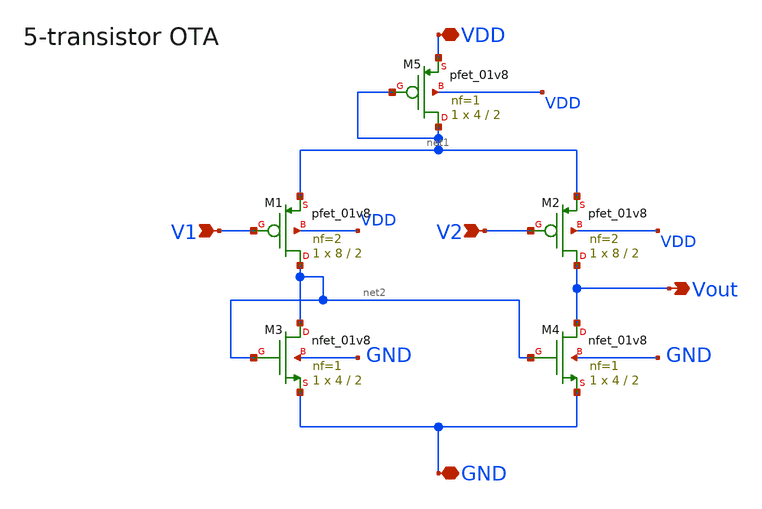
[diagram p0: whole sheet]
** sch_path: src/ota.sch
**.subckt ota VDD GND V2 V1 Vout
*.iopin VDD
*.iopin GND
*.ipin V2
*.ipin V1
*.opin Vout
XM1 net2 V1 net1 VDD sky130_fd_pr__pfet_01v8 L=2 W=8 nf=2 ad='int((2 + 1)/2) * 8 / 2 * 0.29' as='int((2 + 2)/2) * 8 / 2 * 0.29'
+ pd='2*int((2 + 1)/2) * (8 / 2 + 0.29)' ps='2*int((2 + 2)/2) * (8 / 2 + 0.29)' nrd='0.29 / 8 ' nrs='0.29 / 8 '
+ sa=0 sb=0 sd=0 mult=1 m=1
XM3 net2 net2 GND GND sky130_fd_pr__nfet_01v8 L=2 W=4 nf=1 ad='int((1 + 1)/2) * 4 / 1 * 0.29' as='int((1 + 2)/2) * 4 / 1 * 0.29'
+ pd='2*int((1 + 1)/2) * (4 / 1 + 0.29)' ps='2*int((1 + 2)/2) * (4 / 1 + 0.29)' nrd='0.29 / 4 ' nrs='0.29 / 4 '
+ sa=0 sb=0 sd=0 mult=1 m=1
XM4 Vout net2 GND GND sky130_fd_pr__nfet_01v8 L=2 W=4 nf=1 ad='int((1 + 1)/2) * 4 / 1 * 0.29' as='int((1 + 2)/2) * 4 / 1 * 0.29'
+ pd='2*int((1 + 1)/2) * (4 / 1 + 0.29)' ps='2*int((1 + 2)/2) * (4 / 1 + 0.29)' nrd='0.29 / 4 ' nrs='0.29 / 4 '
+ sa=0 sb=0 sd=0 mult=1 m=1
XM2 Vout V2 net1 VDD sky130_fd_pr__pfet_01v8 L=2 W=8 nf=2 ad='int((2 + 1)/2) * 8 / 2 * 0.29' as='int((2 + 2)/2) * 8 / 2 * 0.29'
+ pd='2*int((2 + 1)/2) * (8 / 2 + 0.29)' ps='2*int((2 + 2)/2) * (8 / 2 + 0.29)' nrd='0.29 / 8 ' nrs='0.29 / 8 '
+ sa=0 sb=0 sd=0 mult=1 m=1
XM5 net1 net1 VDD VDD sky130_fd_pr__pfet_01v8 L=2 W=4 nf=1 ad='int((1 + 1)/2) * 4 / 1 * 0.29' as='int((1 + 2)/2) * 4 / 1 * 0.29'
+ pd='2*int((1 + 1)/2) * (4 / 1 + 0.29)' ps='2*int((1 + 2)/2) * (4 / 1 + 0.29)' nrd='0.29 / 4 ' nrs='0.29 / 4 '
+ sa=0 sb=0 sd=0 mult=1 m=1
**** begin user architecture code

**** end user architecture code
**.ends
.end
